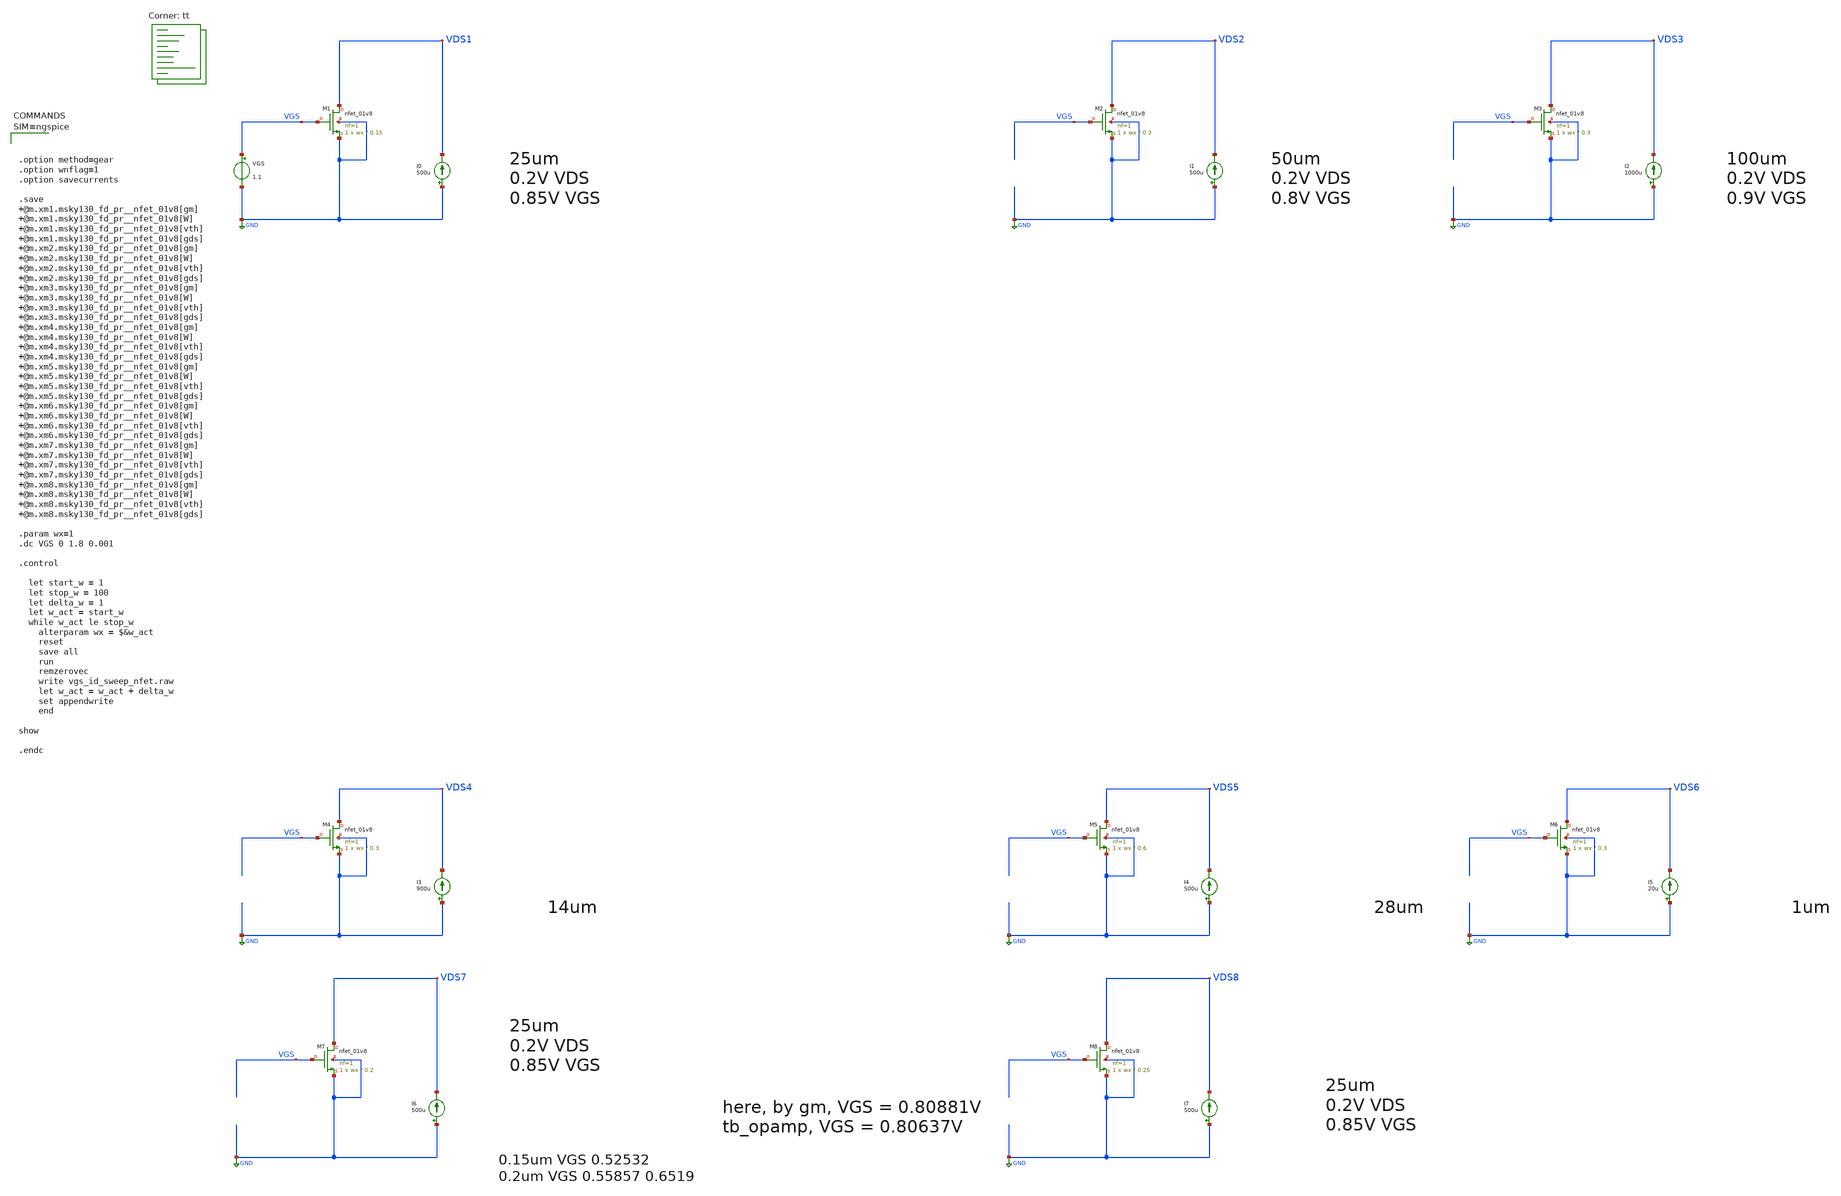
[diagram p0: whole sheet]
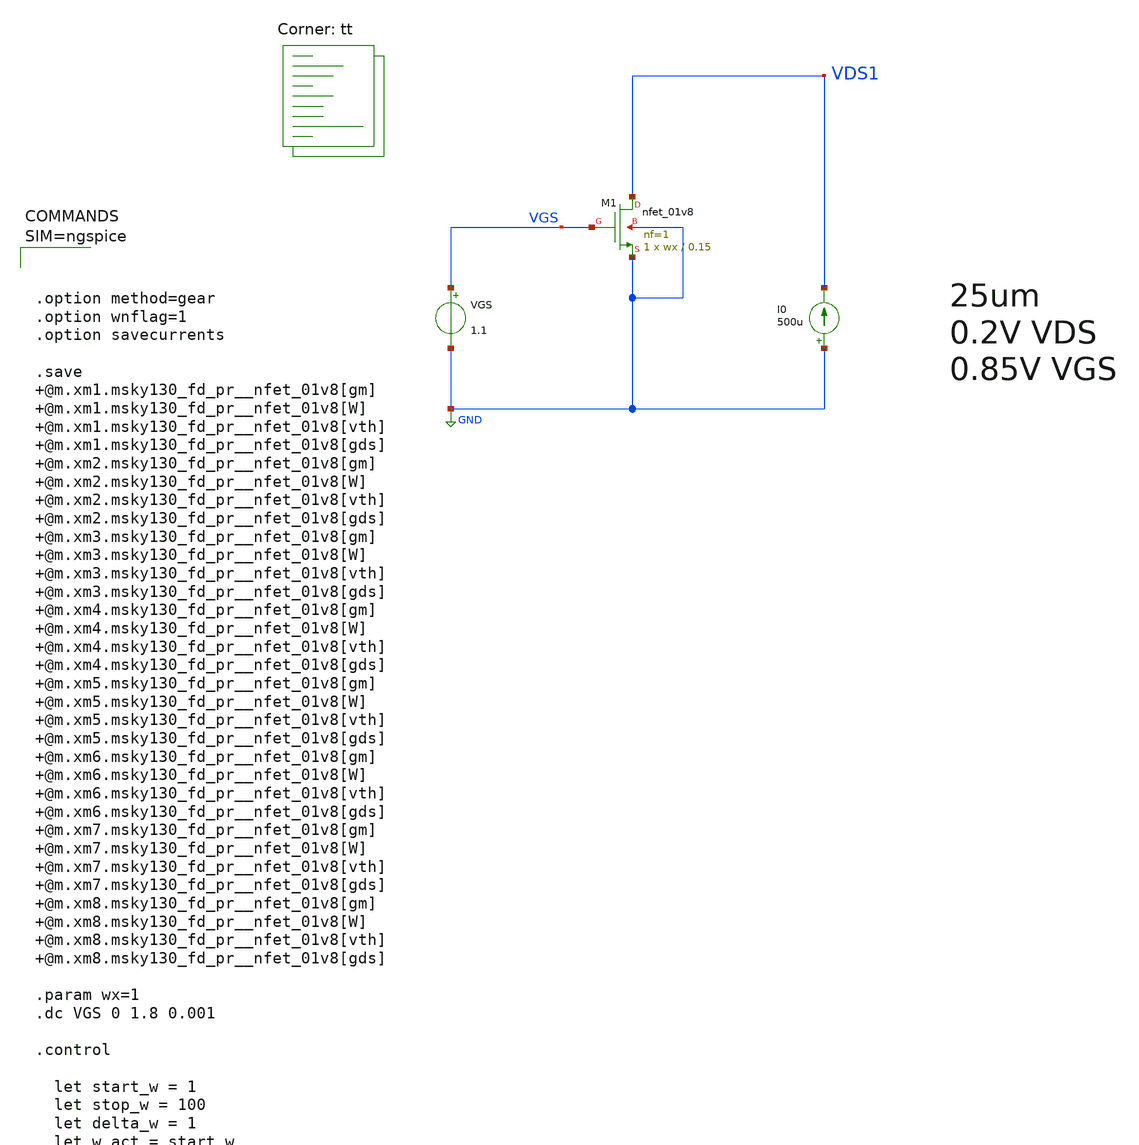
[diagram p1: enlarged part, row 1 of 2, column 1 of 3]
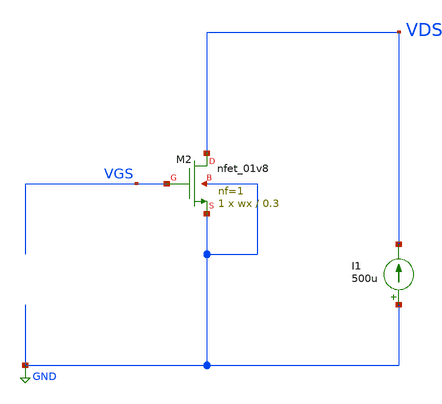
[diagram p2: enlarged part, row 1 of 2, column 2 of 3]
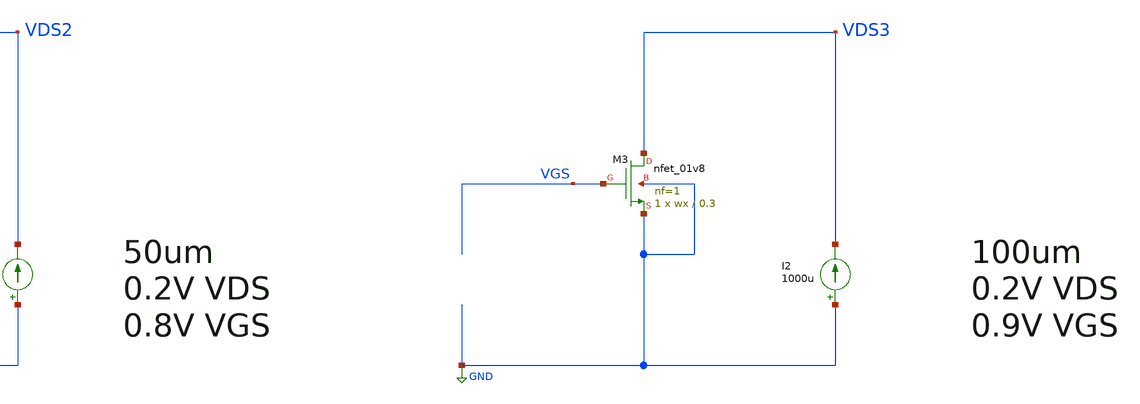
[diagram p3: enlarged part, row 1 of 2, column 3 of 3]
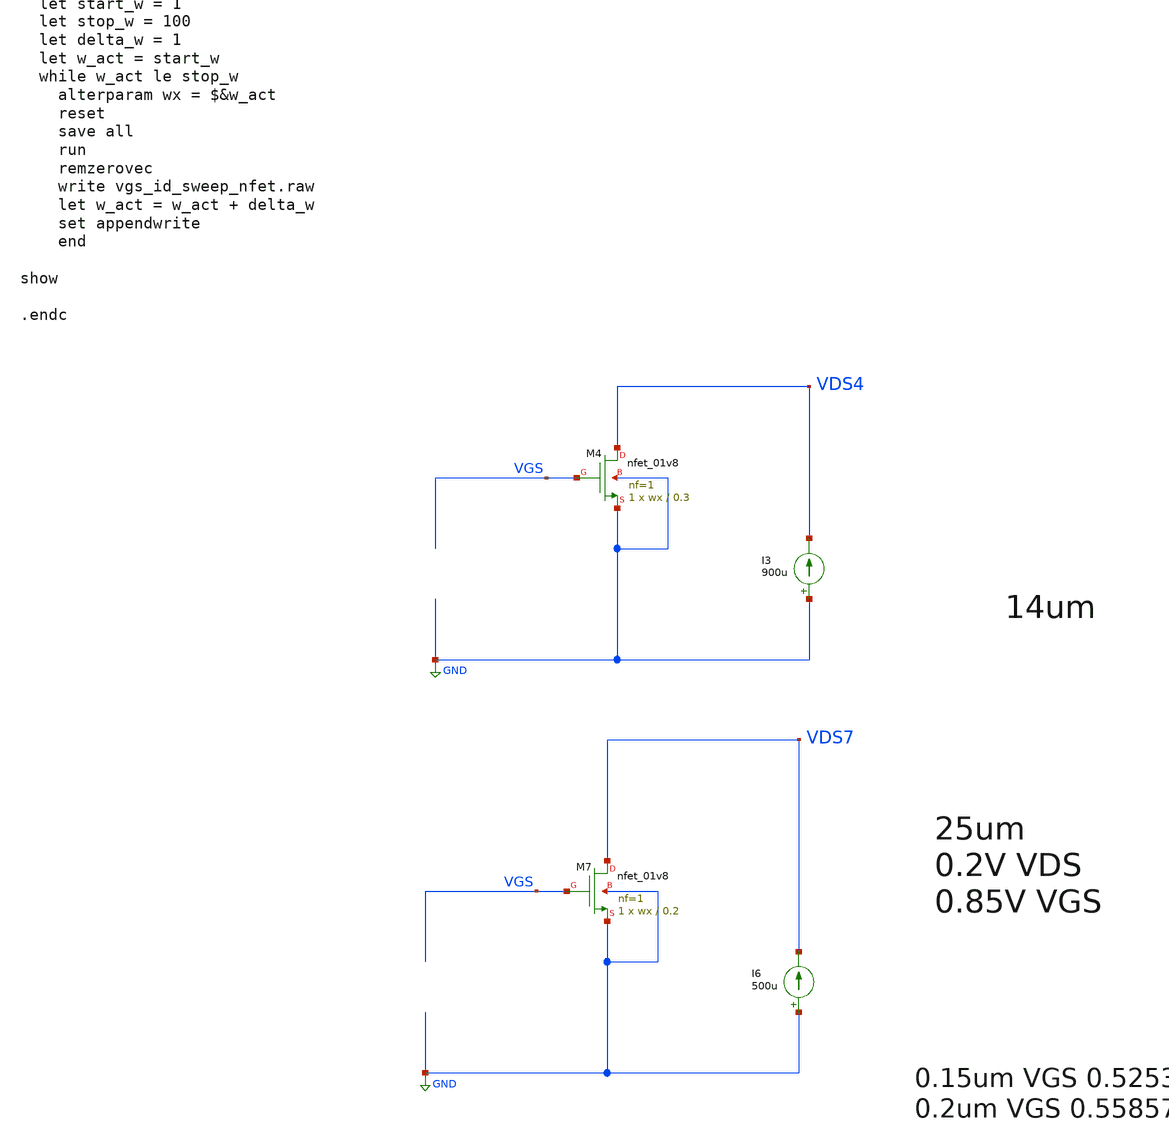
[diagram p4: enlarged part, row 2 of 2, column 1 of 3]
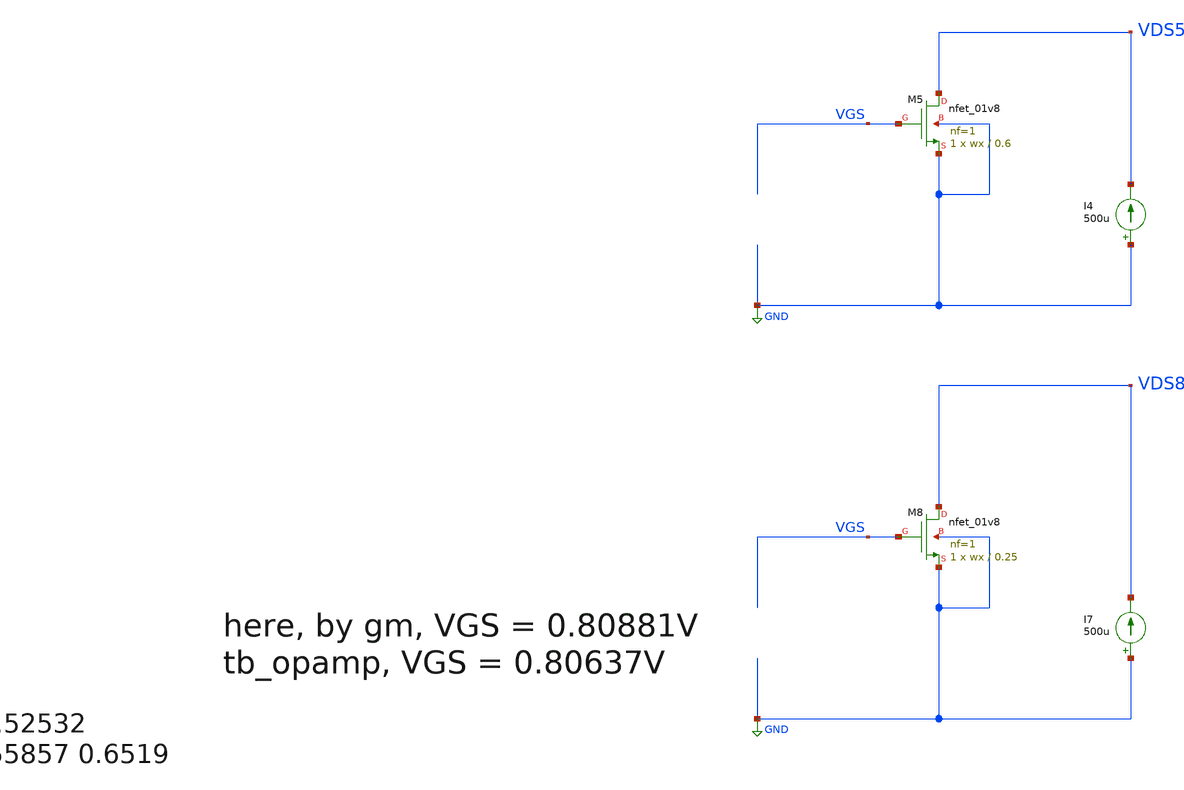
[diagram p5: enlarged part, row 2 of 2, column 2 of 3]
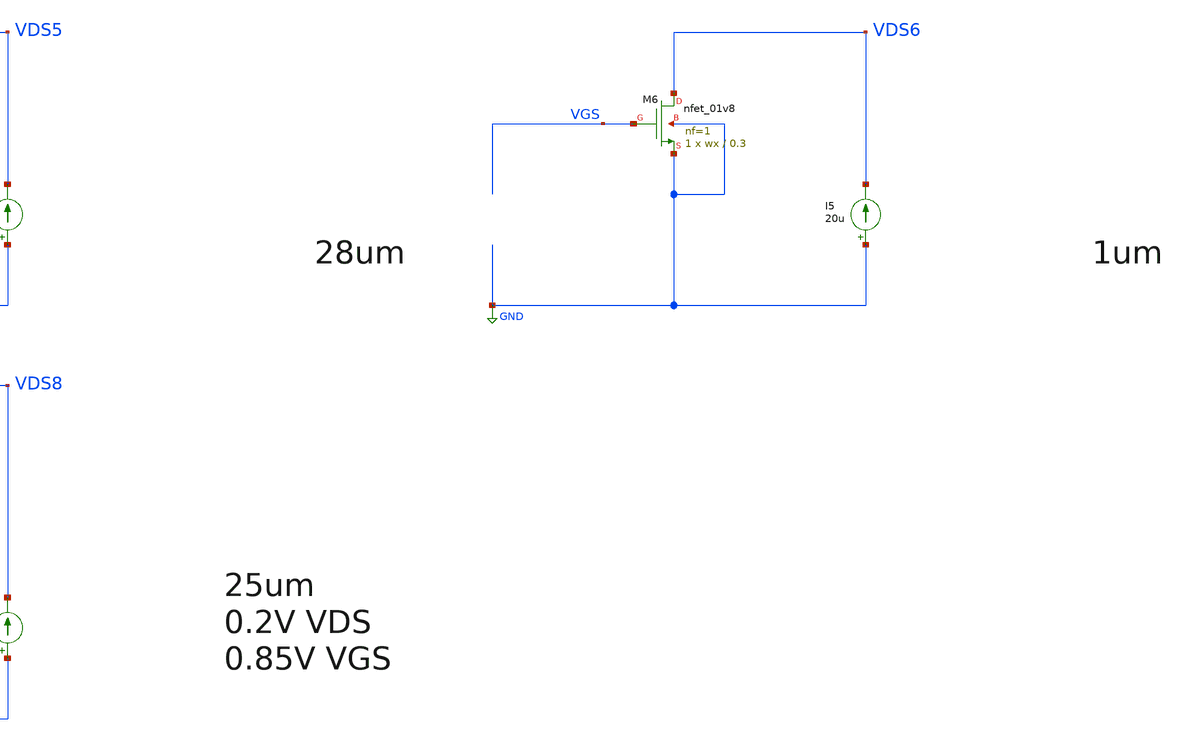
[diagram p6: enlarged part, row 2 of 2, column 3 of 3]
** sch_path: projects/opamp/xschem_ngspice/vgs_id_sweep_nfet.sch
**.subckt vgs_id_sweep_nfet
XM1 VDS1 VGS GND GND sky130_fd_pr__nfet_01v8 L=0.15 W=wx nf=1 ad='int((nf+1)/2) * W/nf * 0.29' as='int((nf+2)/2) * W/nf * 0.29'
+ pd='2*int((nf+1)/2) * (W/nf + 0.29)' ps='2*int((nf+2)/2) * (W/nf + 0.29)' nrd='0.29 / W' nrs='0.29 / W'
+ sa=0 sb=0 sd=0 mult=1 m=1
VGS VGS GND 1.1
I0 GND VDS1 500u
XM2 VDS2 VGS GND GND sky130_fd_pr__nfet_01v8 L=0.3 W=wx nf=1 ad='int((nf+1)/2) * W/nf * 0.29' as='int((nf+2)/2) * W/nf * 0.29'
+ pd='2*int((nf+1)/2) * (W/nf + 0.29)' ps='2*int((nf+2)/2) * (W/nf + 0.29)' nrd='0.29 / W' nrs='0.29 / W'
+ sa=0 sb=0 sd=0 mult=1 m=1
I1 GND VDS2 500u
XM3 VDS3 VGS GND GND sky130_fd_pr__nfet_01v8 L=0.3 W=wx nf=1 ad='int((nf+1)/2) * W/nf * 0.29' as='int((nf+2)/2) * W/nf * 0.29'
+ pd='2*int((nf+1)/2) * (W/nf + 0.29)' ps='2*int((nf+2)/2) * (W/nf + 0.29)' nrd='0.29 / W' nrs='0.29 / W'
+ sa=0 sb=0 sd=0 mult=1 m=1
I2 GND VDS3 1000u
XM4 VDS4 VGS GND GND sky130_fd_pr__nfet_01v8 L=0.3 W=wx nf=1 ad='int((nf+1)/2) * W/nf * 0.29' as='int((nf+2)/2) * W/nf * 0.29'
+ pd='2*int((nf+1)/2) * (W/nf + 0.29)' ps='2*int((nf+2)/2) * (W/nf + 0.29)' nrd='0.29 / W' nrs='0.29 / W'
+ sa=0 sb=0 sd=0 mult=1 m=1
I3 GND VDS4 900u
XM5 VDS5 VGS GND GND sky130_fd_pr__nfet_01v8 L=0.6 W=wx nf=1 ad='int((nf+1)/2) * W/nf * 0.29' as='int((nf+2)/2) * W/nf * 0.29'
+ pd='2*int((nf+1)/2) * (W/nf + 0.29)' ps='2*int((nf+2)/2) * (W/nf + 0.29)' nrd='0.29 / W' nrs='0.29 / W'
+ sa=0 sb=0 sd=0 mult=1 m=1
I4 GND VDS5 500u
XM6 VDS6 VGS GND GND sky130_fd_pr__nfet_01v8 L=0.3 W=wx nf=1 ad='int((nf+1)/2) * W/nf * 0.29' as='int((nf+2)/2) * W/nf * 0.29'
+ pd='2*int((nf+1)/2) * (W/nf + 0.29)' ps='2*int((nf+2)/2) * (W/nf + 0.29)' nrd='0.29 / W' nrs='0.29 / W'
+ sa=0 sb=0 sd=0 mult=1 m=1
I5 GND VDS6 20u
XM7 VDS7 VGS GND GND sky130_fd_pr__nfet_01v8 L=0.2 W=wx nf=1 ad='int((nf+1)/2) * W/nf * 0.29' as='int((nf+2)/2) * W/nf * 0.29'
+ pd='2*int((nf+1)/2) * (W/nf + 0.29)' ps='2*int((nf+2)/2) * (W/nf + 0.29)' nrd='0.29 / W' nrs='0.29 / W'
+ sa=0 sb=0 sd=0 mult=1 m=1
I6 GND VDS7 500u
XM8 VDS8 VGS GND GND sky130_fd_pr__nfet_01v8 L=0.25 W=wx nf=1 ad='int((nf+1)/2) * W/nf * 0.29' as='int((nf+2)/2) * W/nf * 0.29'
+ pd='2*int((nf+1)/2) * (W/nf + 0.29)' ps='2*int((nf+2)/2) * (W/nf + 0.29)' nrd='0.29 / W' nrs='0.29 / W'
+ sa=0 sb=0 sd=0 mult=1 m=1
I7 GND VDS8 500u
**** begin user architecture code
.lib $::SKYWATER_MODELS/sky130.lib.spice tt




.option method=gear
.option wnflag=1
.option savecurrents

.save @m.xm1.msky130_fd_pr__nfet_01v8[gm] @m.xm1.msky130_fd_pr__nfet_01v8[W] @m.xm1.msky130_fd_pr__nfet_01v8[vth] @m.xm1.msky130_fd_pr__nfet_01v8[gds] @m.xm2.msky130_fd_pr__nfet_01v8[gm] @m.xm2.msky130_fd_pr__nfet_01v8[W] @m.xm2.msky130_fd_pr__nfet_01v8[vth] @m.xm2.msky130_fd_pr__nfet_01v8[gds] @m.xm3.msky130_fd_pr__nfet_01v8[gm] @m.xm3.msky130_fd_pr__nfet_01v8[W] @m.xm3.msky130_fd_pr__nfet_01v8[vth] @m.xm3.msky130_fd_pr__nfet_01v8[gds] @m.xm4.msky130_fd_pr__nfet_01v8[gm] @m.xm4.msky130_fd_pr__nfet_01v8[W] @m.xm4.msky130_fd_pr__nfet_01v8[vth] @m.xm4.msky130_fd_pr__nfet_01v8[gds] @m.xm5.msky130_fd_pr__nfet_01v8[gm] @m.xm5.msky130_fd_pr__nfet_01v8[W] @m.xm5.msky130_fd_pr__nfet_01v8[vth] @m.xm5.msky130_fd_pr__nfet_01v8[gds] @m.xm6.msky130_fd_pr__nfet_01v8[gm] @m.xm6.msky130_fd_pr__nfet_01v8[W] @m.xm6.msky130_fd_pr__nfet_01v8[vth] @m.xm6.msky130_fd_pr__nfet_01v8[gds] @m.xm7.msky130_fd_pr__nfet_01v8[gm] @m.xm7.msky130_fd_pr__nfet_01v8[W] @m.xm7.msky130_fd_pr__nfet_01v8[vth] @m.xm7.msky130_fd_pr__nfet_01v8[gds] @m.xm8.msky130_fd_pr__nfet_01v8[gm] @m.xm8.msky130_fd_pr__nfet_01v8[W] @m.xm8.msky130_fd_pr__nfet_01v8[vth] @m.xm8.msky130_fd_pr__nfet_01v8[gds]

.param wx=1
.dc VGS 0 1.8 0.001

.control

  let start_w = 1
  let stop_w = 100
  let delta_w = 1
  let w_act = start_w
  while w_act le stop_w
    alterparam wx = $&w_act
    reset
    save all
    run
    remzerovec
    write vgs_id_sweep_nfet.raw
    let w_act = w_act + delta_w
    set appendwrite
    end

show

.endc




**** end user architecture code
**.ends
.GLOBAL GND
.end
